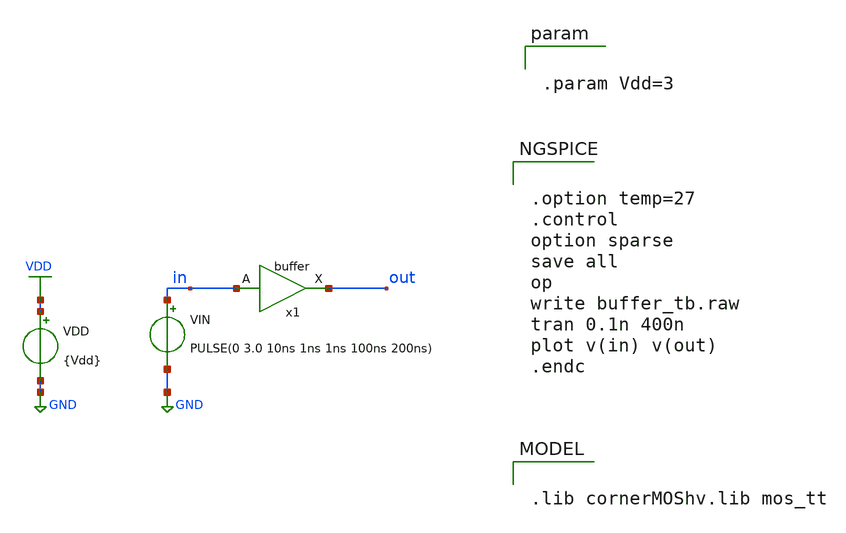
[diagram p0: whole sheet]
** sch_path: 3_real_circuits/buffer_tb.sch
**.subckt buffer_tb
x1 in out buffer
VDD VDD GND {Vdd}
VIN in GND PULSE(0 3.0 10ns 1ns 1ns 100ns 200ns)
**** begin user architecture code


.param Vdd=3




.option temp=27
.control
option sparse
save all
op
write buffer_tb.raw
tran 0.1n 400n
plot v(in) v(out)
.endc



.lib cornerMOShv.lib mos_tt

**** end user architecture code
**.ends

* expanding   symbol:  buffer.sym # of pins=2
** sym_path: 3_real_circuits/buffer.sym
** sch_path: 3_real_circuits/buffer.sch
.subckt buffer A X
*.ipin A
*.opin X
XM2 net1 A GND GND sg13_hv_nmos w=0.3u l=0.45u ng=1 m=1 mm_ok=1
XM1 net1 A VDD VDD sg13_hv_pmos w=0.3u l=0.4u ng=1 m=1 mm_ok=1
XM3 X net1 GND GND sg13_hv_nmos w=0.3u l=0.45u ng=1 m=1 mm_ok=1
XM4 X net1 VDD VDD sg13_hv_pmos w=0.3u l=0.4u ng=1 m=1 mm_ok=1
.ends

.GLOBAL VDD
.GLOBAL GND
.end
